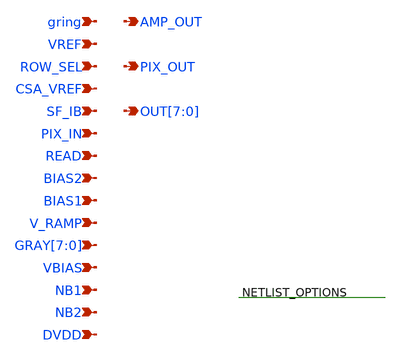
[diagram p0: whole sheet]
** sch_path: xschem/post_layout/pixel_layout.sch
**.subckt pixel_layout AMP_OUT gring VREF ROW_SEL PIX_OUT CSA_VREF SF_IB PIX_IN READ BIAS2 BIAS1
*+ V_RAMP GRAY[7],GRAY[6],GRAY[5],GRAY[4],GRAY[3],GRAY[2],GRAY[1],GRAY[0] VBIAS NB1 NB2 DVDD
*+ OUT[7],OUT[6],OUT[5],OUT[4],OUT[3],OUT[2],OUT[1],OUT[0]
*.opin AMP_OUT
*.ipin gring
*.ipin VREF
*.ipin ROW_SEL
*.opin PIX_OUT
*.ipin CSA_VREF
*.ipin SF_IB
*.ipin PIX_IN
*.ipin READ
*.ipin BIAS2
*.ipin BIAS1
*.ipin V_RAMP
*.ipin GRAY[7],GRAY[6],GRAY[5],GRAY[4],GRAY[3],GRAY[2],GRAY[1],GRAY[0]
*.ipin VBIAS
*.ipin NB1
*.ipin NB2
*.ipin DVDD
*.opin OUT[7],OUT[6],OUT[5],OUT[4],OUT[3],OUT[2],OUT[1],OUT[0]
**.ends
**** begin user architecture code


X8bit_dram_0 READ GRAYx2x OUTx4x OUTx2x OUTx6x GRAYx3x GRAYx4x OUTx0x GRAYx1x OUTx7x  GRAYx5x OUTx3x
+ GRAYx7x 8bit_dram_0/4bit_dram_1/dram_array_1/dram_cell_1/WWL OUTx5x  OUTx1x GRAYx6x GND GRAYx0x x8bit_dram
X0 a_2200_n380# ROW_SEL PIX_OUT GND sky130_fd_pr__nfet_01v8_lvt ad=6.5e+11p pd=5e+06u as=1e+12p
+ ps=5e+06u w=2e+06u l=1e+06u
X1 DVDD a_1000_n1450# a_1000_n1450# DVDD sky130_fd_pr__pfet_01v8_lvt ad=1.45e+12p pd=1.09e+07u
+ as=3.5e+11p ps=2.7e+06u w=1e+06u l=1e+06u
X2 8bit_dram_0/4bit_dram_1/dram_array_1/dram_cell_1/WWL a_1870_n1400# GND GND
+ sky130_fd_pr__nfet_01v8 ad=4e+11p pd=2.8e+06u as=8.70025e+11p ps=7.105e+06u w=1e+06u l=150000u
X3 GND NB1 a_n30_n2640# GND sky130_fd_pr__nfet_01v8_lvt ad=0p pd=0u as=3.22e+12p ps=1.79e+07u
+ w=1.2e+06u l=1e+06u
X4 a_n140_n550# VBIAS a_n140_n780# GND sky130_fd_pr__nfet_01v8_lvt ad=3.5e+11p pd=2.7e+06u
+ as=2.1525e+12p ps=1.76e+07u w=1e+06u l=800000u
X5 a_1720_n1450# V_RAMP a_1100_n1450# GND sky130_fd_pr__nfet_01v8_lvt ad=3.5e+11p pd=2.7e+06u
+ as=8.8e+11p ps=7.1e+06u w=1e+06u l=150000u
X6 a_1870_n1400# a_1720_n1450# DVDD DVDD sky130_fd_pr__pfet_01v8_lvt ad=3.5e+11p pd=2.7e+06u as=0p
+ ps=0u w=1e+06u l=450000u
X7 a_1100_n1450# AMP_OUT a_1000_n1450# GND sky130_fd_pr__nfet_01v8_lvt ad=0p pd=0u as=3.5e+11p
+ ps=2.7e+06u w=1e+06u l=150000u
X8 a_2287_n292# AMP_OUT GND VDD sky130_fd_pr__pfet_01v8_lvt ad=5e+11p pd=3e+06u as=3.50025e+11p
+ ps=2.705e+06u w=1e+06u l=1e+06u
X9 8bit_dram_0/4bit_dram_1/dram_array_1/dram_cell_1/WWL a_1870_n1400# DVDD DVDD
+ sky130_fd_pr__pfet_01v8 ad=3.5e+11p pd=2.7e+06u as=0p ps=0u w=1e+06u l=200000u
X10 AMP_OUT NB2 GND GND sky130_fd_pr__nfet_01v8_lvt ad=6.975e+11p pd=5.7e+06u as=0p ps=0u w=1e+06u
+ l=1.2e+06u
X11 a_1100_n1450# BIAS1 GND GND sky130_fd_pr__nfet_01v8 ad=0p pd=0u as=0p ps=0u w=450000u l=1e+06u
X12 a_350_10# a_n140_n550# a_n140_n550# VDD sky130_fd_pr__pfet_01v8_lvt ad=3.5e+11p pd=2.7e+06u
+ as=3.5e+11p ps=2.7e+06u w=1e+06u l=2e+06u
X13 VDD SF_IB a_2287_n292# VDD sky130_fd_pr__pfet_01v8_lvt ad=1.05e+12p pd=8.1e+06u as=0p ps=0u
+ w=1e+06u l=1e+06u
X14 PIX_IN AMP_OUT sky130_fd_pr__cap_mim_m3_1 l=2e+06u w=2e+06u
X15 a_n30_n2640# VREF a_n140_n780# GND sky130_fd_pr__nfet_01v8_lvt ad=0p pd=0u as=0p ps=0u w=7e+06u
+ l=150000u
X16 VDD a_350_10# a_350_10# VDD sky130_fd_pr__pfet_01v8_lvt ad=0p pd=0u as=0p ps=0u w=1e+06u
+ l=2e+06u
X17 a_1460_10# a_350_10# VDD VDD sky130_fd_pr__pfet_01v8_lvt ad=3.5e+11p pd=2.7e+06u as=0p ps=0u
+ w=1e+06u l=2e+06u
X18 AMP_OUT CSA_VREF PIX_IN VDD sky130_fd_pr__pfet_01v8_lvt ad=2.94e+11p pd=2.24e+06u as=2.73e+11p
+ ps=2.14e+06u w=420000u l=8e+06u
X19 a_1870_n1400# BIAS2 GND GND sky130_fd_pr__nfet_01v8_lvt ad=3.5e+11p pd=2.7e+06u as=0p ps=0u
+ w=1e+06u l=1e+06u
X20 a_120_n550# a_n140_n550# a_1460_10# VDD sky130_fd_pr__pfet_01v8_lvt ad=3.5e+11p pd=2.7e+06u
+ as=0p ps=0u w=1e+06u l=2e+06u
X21 a_120_n550# VBIAS a_120_n780# GND sky130_fd_pr__nfet_01v8_lvt ad=3.5e+11p pd=2.7e+06u
+ as=2.1525e+12p ps=1.76e+07u w=1e+06u l=800000u
X22 a_120_n780# PIX_IN a_n30_n2640# GND sky130_fd_pr__nfet_01v8_lvt ad=0p pd=0u as=0p ps=0u w=7e+06u
+ l=150000u
X23 a_1720_n1450# a_1000_n1450# DVDD DVDD sky130_fd_pr__pfet_01v8_lvt ad=3.5e+11p pd=2.7e+06u as=0p
+ ps=0u w=1e+06u l=1e+06u
X24 VDD a_120_n550# AMP_OUT GND sky130_fd_pr__nfet_01v8_lvt ad=1.185e+12p pd=8.4e+06u as=0p ps=0u
+ w=1e+06u l=1e+06u
X25 VDD a_2287_n292# a_2200_n380# GND sky130_fd_pr__nfet_01v8_lvt ad=0p pd=0u as=0p ps=0u w=1e+06u
+ l=150000u



.subckt dram_cell storage WWL WBL RWL RBL VSUBS
X0 RWL storage RBL VSUBS sky130_fd_pr__nfet_01v8 ad=3e+11p pd=2.6e+06u as=3.5e+11p ps=2.7e+06u
+ w=1e+06u l=150000u
X1 storage WWL WBL VSUBS sky130_fd_pr__nfet_01v8 ad=3.5e+11p pd=2.7e+06u as=3e+11p ps=2.6e+06u
+ w=1e+06u l=150000u
.ends

.subckt dram_array dram_cell_1/WWL dram_cell_1/RWL dram_cell_0/WBL dram_cell_1/WBL  dram_cell_1/RBL
+ dram_cell_0/RBL VSUBS dram_cell_0/RWL
Xdram_cell_0 dram_cell_0/storage dram_cell_1/WWL dram_cell_0/WBL dram_cell_0/RWL dram_cell_0/RBL
+  VSUBS dram_cell
Xdram_cell_1 dram_cell_1/storage dram_cell_1/WWL dram_cell_1/WBL dram_cell_1/RWL dram_cell_1/RBL
+  VSUBS dram_cell
.ends

.subckt x4bit_dram dram_array_1/dram_cell_0/RWL dram_array_1/dram_cell_0/WBL
+ dram_array_1/dram_cell_1/RWL  dram_array_1/dram_cell_0/RBL dram_array_0/dram_cell_0/RBL dram_array_0/dram_cell_1/WBL
+  dram_array_1/dram_cell_1/WBL dram_array_0/dram_cell_1/RBL dram_array_1/dram_cell_1/RBL  dram_array_0/dram_cell_0/WBL
+ dram_array_1/dram_cell_1/WWL VSUBS
Xdram_array_0 dram_array_1/dram_cell_1/WWL dram_array_1/dram_cell_0/RWL dram_array_0/dram_cell_0/WBL
+  dram_array_0/dram_cell_1/WBL dram_array_0/dram_cell_1/RBL dram_array_0/dram_cell_0/RBL  VSUBS dram_array_1/dram_cell_0/RWL
+ dram_array
Xdram_array_1 dram_array_1/dram_cell_1/WWL dram_array_1/dram_cell_1/RWL dram_array_1/dram_cell_0/WBL
+  dram_array_1/dram_cell_1/WBL dram_array_1/dram_cell_1/RBL dram_array_1/dram_cell_0/RBL  VSUBS dram_array_1/dram_cell_0/RWL
+ dram_array
.ends

.subckt x8bit_dram 4bit_dram_1/dram_array_1/dram_cell_1/RWL 4bit_dram_0/dram_array_1/dram_cell_0/WBL
+  4bit_dram_1/dram_array_0/dram_cell_0/RBL 4bit_dram_0/dram_array_1/dram_cell_0/RBL  4bit_dram_1/dram_array_1/dram_cell_0/RBL
+ 4bit_dram_0/dram_array_1/dram_cell_1/WBL  4bit_dram_1/dram_array_0/dram_cell_0/WBL 4bit_dram_0/dram_array_0/dram_cell_0/RBL
+  4bit_dram_0/dram_array_0/dram_cell_1/WBL 4bit_dram_1/dram_array_1/dram_cell_1/RBL  4bit_dram_1/dram_array_0/dram_cell_1/WBL
+ 4bit_dram_0/dram_array_1/dram_cell_1/RBL  4bit_dram_1/dram_array_1/dram_cell_1/WBL 4bit_dram_1/dram_array_1/dram_cell_1/WWL
+  4bit_dram_1/dram_array_0/dram_cell_1/RBL 4bit_dram_0/dram_array_0/dram_cell_1/RBL  4bit_dram_1/dram_array_1/dram_cell_0/WBL VSUBS
+ 4bit_dram_0/dram_array_0/dram_cell_0/WBL
X4bit_dram_1 4bit_dram_1/dram_array_1/dram_cell_1/RWL 4bit_dram_1/dram_array_1/dram_cell_0/WBL
+  4bit_dram_1/dram_array_1/dram_cell_1/RWL 4bit_dram_1/dram_array_1/dram_cell_0/RBL  4bit_dram_1/dram_array_0/dram_cell_0/RBL
+ 4bit_dram_1/dram_array_0/dram_cell_1/WBL  4bit_dram_1/dram_array_1/dram_cell_1/WBL 4bit_dram_1/dram_array_0/dram_cell_1/RBL
+  4bit_dram_1/dram_array_1/dram_cell_1/RBL 4bit_dram_1/dram_array_0/dram_cell_0/WBL  4bit_dram_1/dram_array_1/dram_cell_1/WWL VSUBS x4bit_dram
X4bit_dram_0 4bit_dram_1/dram_array_1/dram_cell_1/RWL 4bit_dram_0/dram_array_1/dram_cell_0/WBL
+  4bit_dram_1/dram_array_1/dram_cell_1/RWL 4bit_dram_0/dram_array_1/dram_cell_0/RBL  4bit_dram_0/dram_array_0/dram_cell_0/RBL
+ 4bit_dram_0/dram_array_0/dram_cell_1/WBL  4bit_dram_0/dram_array_1/dram_cell_1/WBL 4bit_dram_0/dram_array_0/dram_cell_1/RBL
+  4bit_dram_0/dram_array_1/dram_cell_1/RBL 4bit_dram_0/dram_array_0/dram_cell_0/WBL  4bit_dram_1/dram_array_1/dram_cell_1/WWL VSUBS x4bit_dram
.ends




**** end user architecture code
.end
